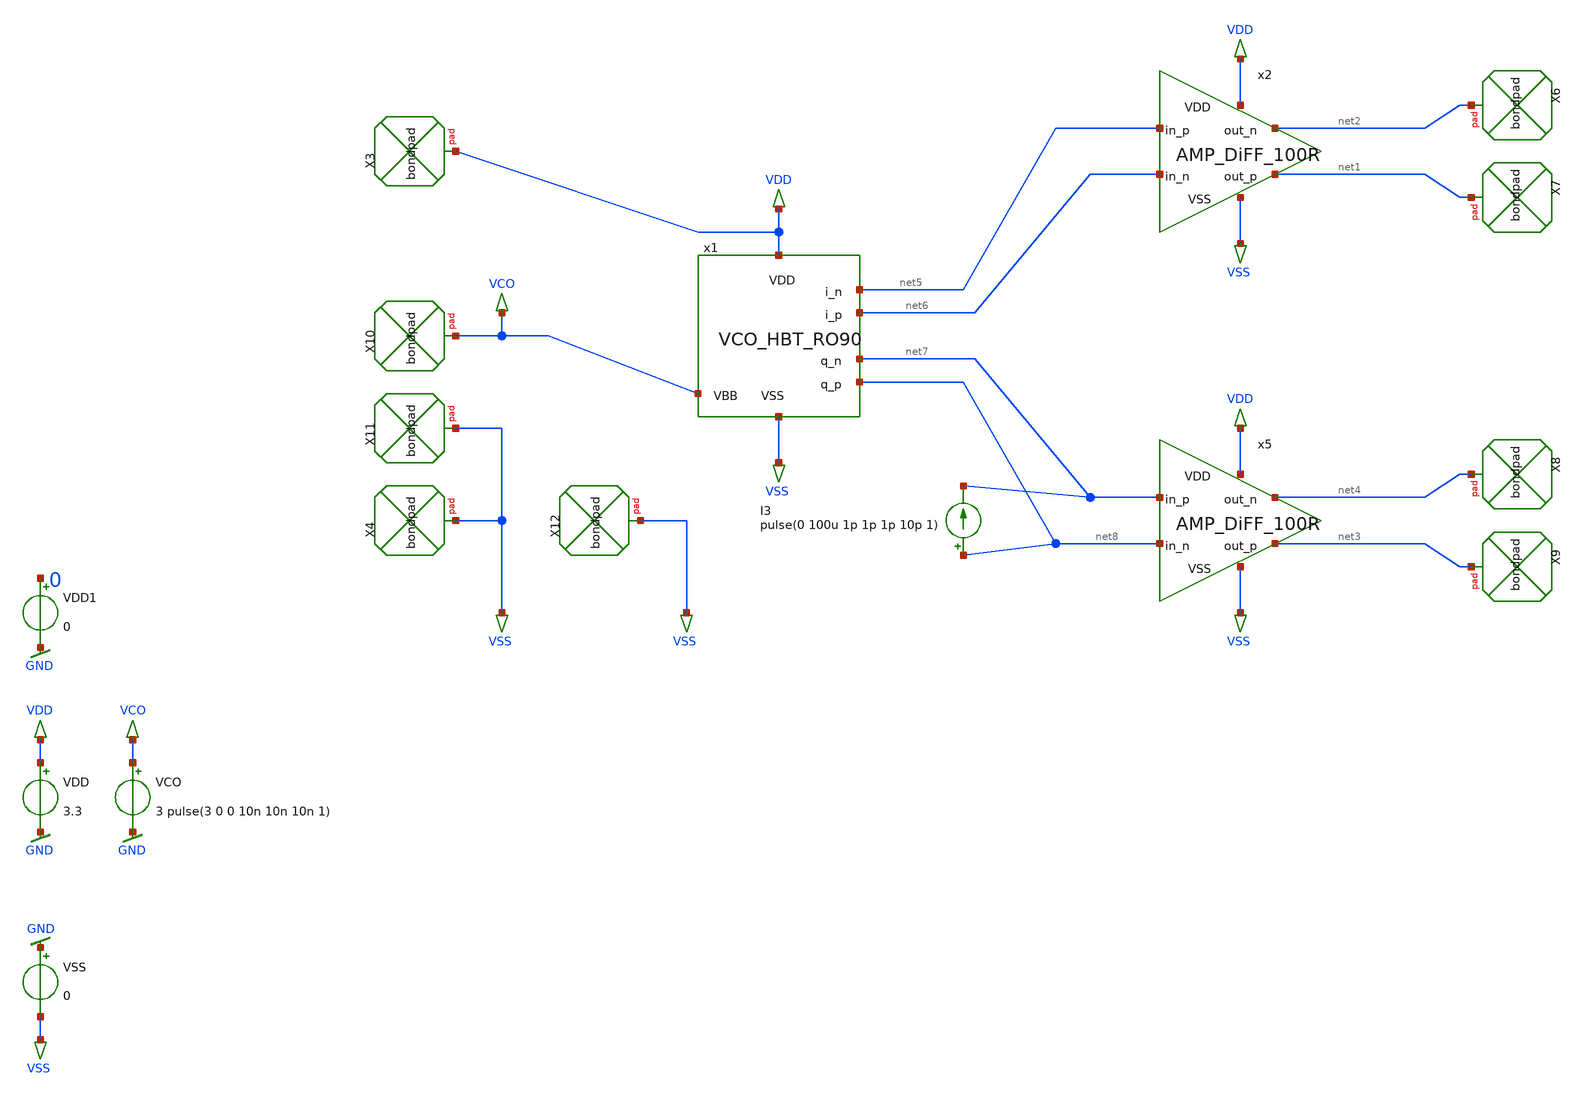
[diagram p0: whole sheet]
** sch_path: HBT_VCO_RO90/design_data/xschem/FMD_QNC_HBT_RO90_mmW.sch
* Copyright (C) 1998-2023 Stefan Frederik Schippers
* This program is free software; you can redistribute it and/or modify
* it under the terms of the GNU General Public License as published by
* the Free Software Foundation; either version 2 of the License, or
* (at your option) any later version.
* This program is distributed in the hope that it will be useful,
* but WITHOUT ANY WARRANTY; without even the implied warranty of
* MERCHANTABILITY or FITNESS FOR A PARTICULAR PURPOSE.  See the
* GNU General Public License for more details.
* You should have received a copy of the GNU General Public License
* along with this program; if not, write to the Free Software
**.subckt FMD_QNC_HBT_RO90_mmW
VDD VDD GND 3.3
VSS GND VSS 0
VDD1 0 GND 0
VCO VCO GND 3 pulse(3 0 0 10n 10n 10n 1)
x2 VDD net5 net1 net6 net2 VSS AMP_DiFF_100R
x5 VDD net7 net3 net8 net4 VSS AMP_DiFF_100R
XX6 net2 bondpad size=80u shape=0 padtype=0
XX7 net1 bondpad size=80u shape=0 padtype=0
XX8 net4 bondpad size=80u shape=0 padtype=0
XX9 net3 bondpad size=80u shape=0 padtype=0
XX10 VCO bondpad size=80u shape=0 padtype=0
I3 net8 net7 pulse(0 100u 1p 1p 1p 10p 1)
x1 net5 net6 VDD net7 net8 VCO VSS VCO_HBT_RO90
XX3 VDD bondpad size=80u shape=0 padtype=0
XX4 VSS bondpad size=80u shape=0 padtype=0
XX11 VSS bondpad size=80u shape=0 padtype=0
XX12 VSS bondpad size=80u shape=0 padtype=0
**** begin user architecture code












**** end user architecture code
**.ends
.GLOBAL GND
.end
